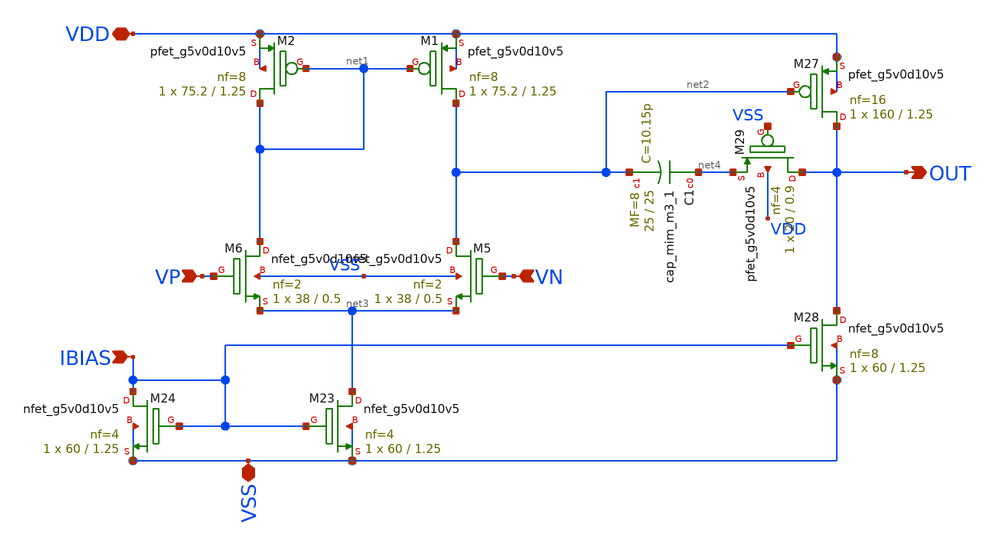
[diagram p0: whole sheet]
** sch_path: opamp_sementara/opamp/opamp_ori.sch
**.subckt opamp_ori VDD VP VN IBIAS VSS OUT
*.iopin VDD
*.ipin VP
*.ipin VN
*.ipin IBIAS
*.iopin VSS
*.opin OUT
XM1 net2 net1 VDD VDD sky130_fd_pr__pfet_g5v0d10v5 L=1.25 W=75.2 nf=8 ad='int((nf+1)/2) * W/nf * 0.29'
+ as='int((nf+2)/2) * W/nf * 0.29' pd='2*int((nf+1)/2) * (W/nf + 0.29)' ps='2*int((nf+2)/2) * (W/nf + 0.29)'
+ nrd='0.29 / W' nrs='0.29 / W' sa=0 sb=0 sd=0 mult=1 m=1
XM2 net1 net1 VDD VDD sky130_fd_pr__pfet_g5v0d10v5 L=1.25 W=75.2 nf=8 ad='int((nf+1)/2) * W/nf * 0.29'
+ as='int((nf+2)/2) * W/nf * 0.29' pd='2*int((nf+1)/2) * (W/nf + 0.29)' ps='2*int((nf+2)/2) * (W/nf + 0.29)'
+ nrd='0.29 / W' nrs='0.29 / W' sa=0 sb=0 sd=0 mult=1 m=1
XM5 net2 VN net3 VSS sky130_fd_pr__nfet_g5v0d10v5 L=0.5 W=38 nf=2 ad='int((nf+1)/2) * W/nf * 0.29' as='int((nf+2)/2) * W/nf * 0.29'
+ pd='2*int((nf+1)/2) * (W/nf + 0.29)' ps='2*int((nf+2)/2) * (W/nf + 0.29)' nrd='0.29 / W' nrs='0.29 / W'
+ sa=0 sb=0 sd=0 mult=1 m=1
XM6 net1 VP net3 VSS sky130_fd_pr__nfet_g5v0d10v5 L=0.5 W=38 nf=2 ad='int((nf+1)/2) * W/nf * 0.29' as='int((nf+2)/2) * W/nf * 0.29'
+ pd='2*int((nf+1)/2) * (W/nf + 0.29)' ps='2*int((nf+2)/2) * (W/nf + 0.29)' nrd='0.29 / W' nrs='0.29 / W'
+ sa=0 sb=0 sd=0 mult=1 m=1
XM23 net3 IBIAS VSS VSS sky130_fd_pr__nfet_g5v0d10v5 L=1.25 W=60 nf=4 ad='int((nf+1)/2) * W/nf * 0.29'
+ as='int((nf+2)/2) * W/nf * 0.29' pd='2*int((nf+1)/2) * (W/nf + 0.29)' ps='2*int((nf+2)/2) * (W/nf + 0.29)'
+ nrd='0.29 / W' nrs='0.29 / W' sa=0 sb=0 sd=0 mult=1 m=1
XM24 IBIAS IBIAS VSS VSS sky130_fd_pr__nfet_g5v0d10v5 L=1.25 W=60 nf=4 ad='int((nf+1)/2) * W/nf * 0.29'
+ as='int((nf+2)/2) * W/nf * 0.29' pd='2*int((nf+1)/2) * (W/nf + 0.29)' ps='2*int((nf+2)/2) * (W/nf + 0.29)'
+ nrd='0.29 / W' nrs='0.29 / W' sa=0 sb=0 sd=0 mult=1 m=1
XM27 OUT net2 VDD VDD sky130_fd_pr__pfet_g5v0d10v5 L=1.25 W=160 nf=16 ad='int((nf+1)/2) * W/nf * 0.29'
+ as='int((nf+2)/2) * W/nf * 0.29' pd='2*int((nf+1)/2) * (W/nf + 0.29)' ps='2*int((nf+2)/2) * (W/nf + 0.29)'
+ nrd='0.29 / W' nrs='0.29 / W' sa=0 sb=0 sd=0 mult=1 m=1
XM28 OUT IBIAS VSS VSS sky130_fd_pr__nfet_g5v0d10v5 L=1.25 W=60 nf=8 ad='int((nf+1)/2) * W/nf * 0.29'
+ as='int((nf+2)/2) * W/nf * 0.29' pd='2*int((nf+1)/2) * (W/nf + 0.29)' ps='2*int((nf+2)/2) * (W/nf + 0.29)'
+ nrd='0.29 / W' nrs='0.29 / W' sa=0 sb=0 sd=0 mult=1 m=1
XC1 net4 net2 sky130_fd_pr__cap_mim_m3_1 W=25 L=25 MF=8 m=8
XM29 OUT VSS net4 VDD sky130_fd_pr__pfet_g5v0d10v5 L=0.9 W=20 nf=4 ad='int((nf+1)/2) * W/nf * 0.29' as='int((nf+2)/2) * W/nf * 0.29'
+ pd='2*int((nf+1)/2) * (W/nf + 0.29)' ps='2*int((nf+2)/2) * (W/nf + 0.29)' nrd='0.29 / W' nrs='0.29 / W'
+ sa=0 sb=0 sd=0 mult=1 m=1
**.ends
.end
